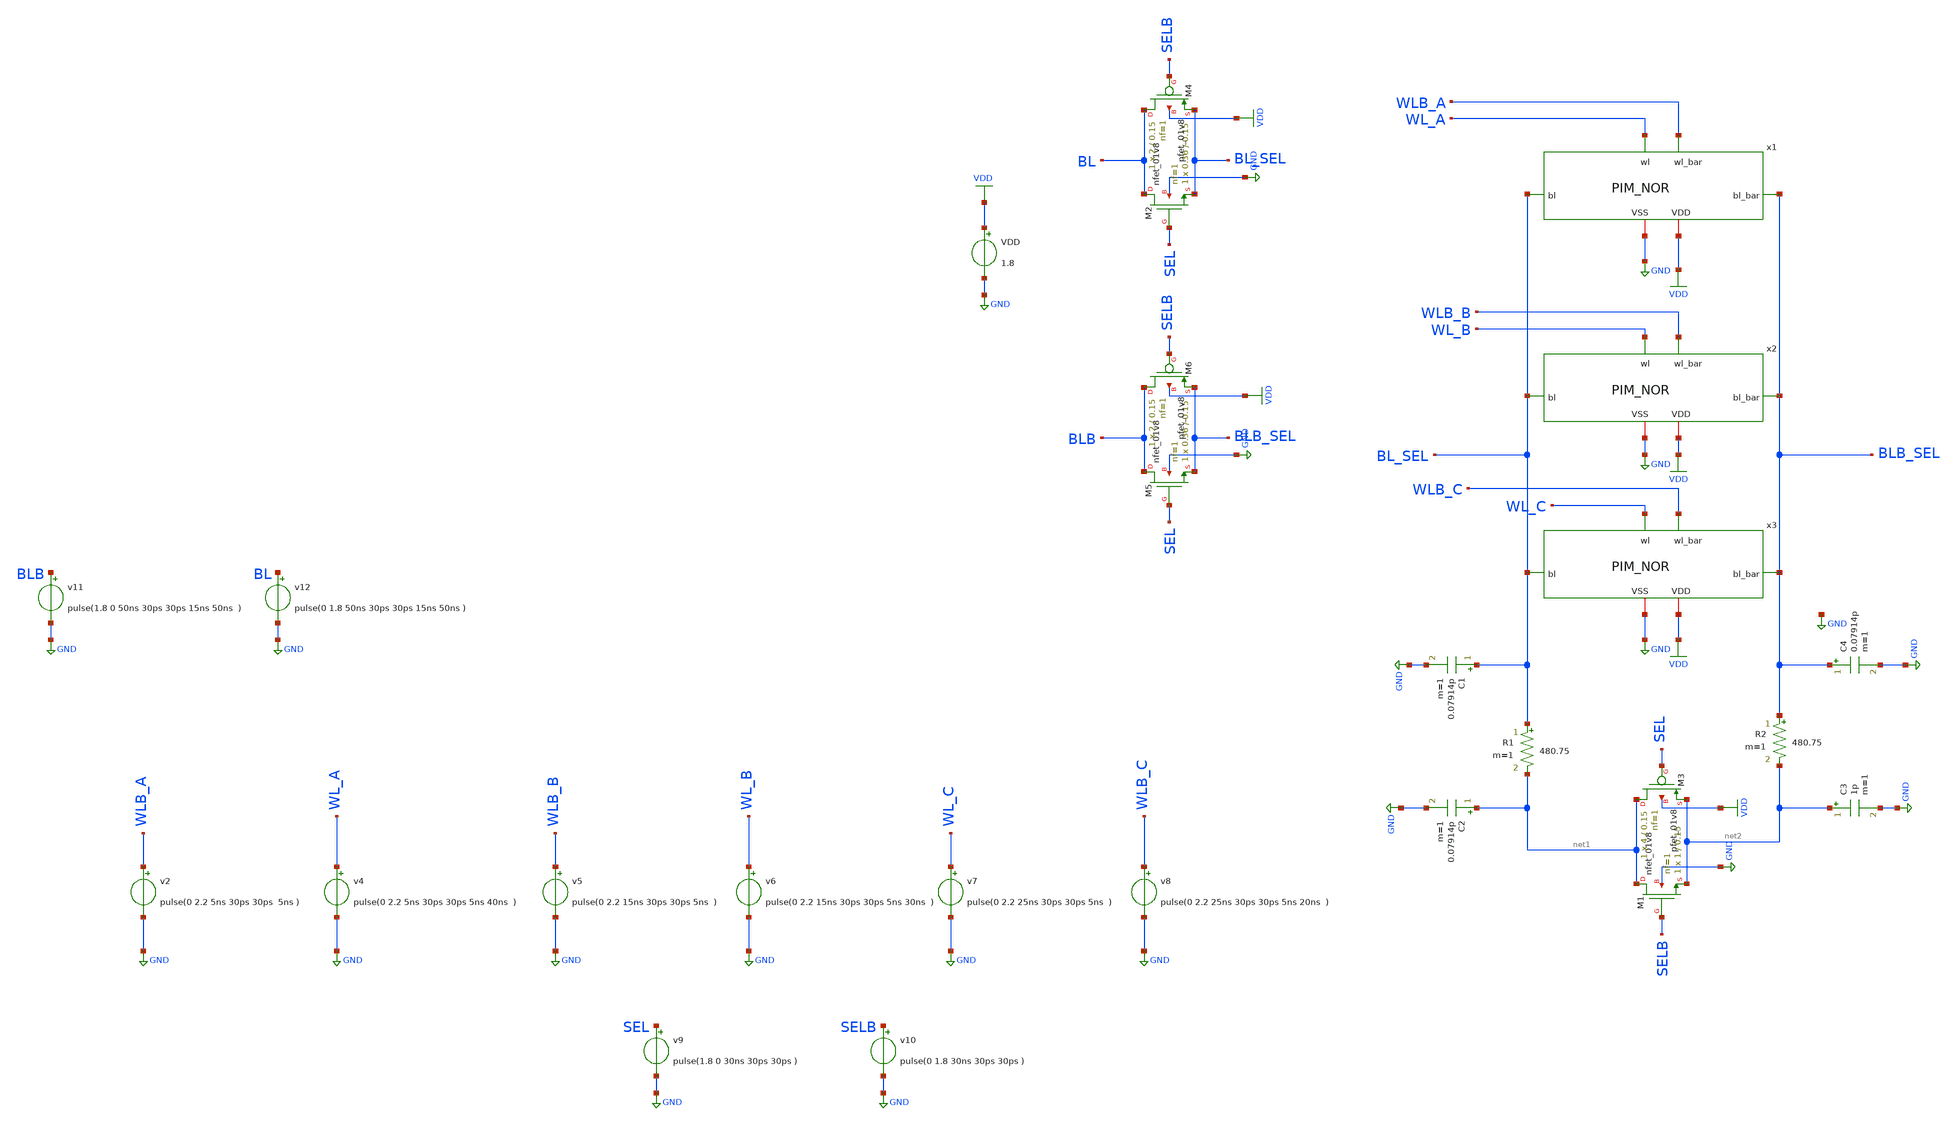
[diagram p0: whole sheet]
** sch_path: nikhil/SRAM/NAND_DEMO_3_res_test_00.sch
**.subckt NAND_DEMO_3_res_test_00
x1 WL_A WLB_A VDD BL_SEL BLB_SEL GND PIM_NOR
x2 WL_B WLB_B VDD BL_SEL BLB_SEL GND PIM_NOR
x3 WL_C WLB_C VDD BL_SEL BLB_SEL GND PIM_NOR
VDD VDD GND 1.8
XM2 BL SEL BL_SEL GND sky130_fd_pr__nfet_01v8 L=0.15 W=0.36 nf=1 ad='int((nf+1)/2) * W/nf * 0.29' as='int((nf+2)/2) * W/nf * 0.29'
+ pd='2*int((nf+1)/2) * (W/nf + 0.29)' ps='2*int((nf+2)/2) * (W/nf + 0.29)' nrd='0.29 / W' nrs='0.29 / W'
+ sa=0 sb=0 sd=0 mult=1 m=1
XM4 BL SELB BL_SEL VDD sky130_fd_pr__pfet_01v8 L=0.15 W=2 nf=1 ad='int((nf+1)/2) * W/nf * 0.29' as='int((nf+2)/2) * W/nf * 0.29'
+ pd='2*int((nf+1)/2) * (W/nf + 0.29)' ps='2*int((nf+2)/2) * (W/nf + 0.29)' nrd='0.29 / W' nrs='0.29 / W'
+ sa=0 sb=0 sd=0 mult=1 m=1
XM5 BLB SEL BLB_SEL GND sky130_fd_pr__nfet_01v8 L=0.15 W=0.36 nf=1 ad='int((nf+1)/2) * W/nf * 0.29' as='int((nf+2)/2) * W/nf * 0.29'
+ pd='2*int((nf+1)/2) * (W/nf + 0.29)' ps='2*int((nf+2)/2) * (W/nf + 0.29)' nrd='0.29 / W' nrs='0.29 / W'
+ sa=0 sb=0 sd=0 mult=1 m=1
XM6 BLB SELB BLB_SEL VDD sky130_fd_pr__pfet_01v8 L=0.15 W=2 nf=1 ad='int((nf+1)/2) * W/nf * 0.29' as='int((nf+2)/2) * W/nf * 0.29'
+ pd='2*int((nf+1)/2) * (W/nf + 0.29)' ps='2*int((nf+2)/2) * (W/nf + 0.29)' nrd='0.29 / W' nrs='0.29 / W'
+ sa=0 sb=0 sd=0 mult=1 m=1
v2 WLB_A GND pulse(0 2.2 5ns 30ps 30ps 5ns )
v4 WL_A GND pulse(0 2.2 5ns 30ps 30ps 5ns 40ns )
v5 WLB_B GND pulse(0 2.2 15ns 30ps 30ps 5ns )
v6 WL_B GND pulse(0 2.2 15ns 30ps 30ps 5ns 30ns )
v7 WL_C GND pulse(0 2.2 25ns 30ps 30ps 5ns )
v8 WLB_C GND pulse(0 2.2 25ns 30ps 30ps 5ns 20ns )
v9 SEL GND pulse(1.8 0 30ns 30ps 30ps )
v10 SELB GND pulse(0 1.8 30ns 30ps 30ps )
XM1 net1 SELB net2 GND sky130_fd_pr__nfet_01v8 L=0.15 W=1 nf=1 ad='int((nf+1)/2) * W/nf * 0.29' as='int((nf+2)/2) * W/nf * 0.29'
+ pd='2*int((nf+1)/2) * (W/nf + 0.29)' ps='2*int((nf+2)/2) * (W/nf + 0.29)' nrd='0.29 / W' nrs='0.29 / W'
+ sa=0 sb=0 sd=0 mult=1 m=1
XM3 net1 SEL net2 VDD sky130_fd_pr__pfet_01v8 L=0.15 W=4 nf=1 ad='int((nf+1)/2) * W/nf * 0.29' as='int((nf+2)/2) * W/nf * 0.29'
+ pd='2*int((nf+1)/2) * (W/nf + 0.29)' ps='2*int((nf+2)/2) * (W/nf + 0.29)' nrd='0.29 / W' nrs='0.29 / W'
+ sa=0 sb=0 sd=0 mult=1 m=1
C1 BL_SEL GND 0.07914p m=1
R1 BL_SEL net1 480.75 m=1
R2 BLB_SEL net2 480.75 m=1
C2 net1 GND 0.07914p m=1
C3 net2 GND 1p m=1
C4 BLB_SEL GND 0.07914p m=1
v11 BLB GND pulse(1.8 0 50ns 30ps 30ps 15ns 50ns )
v12 BL GND pulse(0 1.8 50ns 30ps 30ps 15ns 50ns )
**** begin user architecture code

.tran


.options wnflag=1
.include /pdk/open_pdks/sources/sky130-pdk/libraries/sky130_fd_pr/latest/cells/nfet_01v8/sky130_fd_pr__nfet_01v8__tt.corner.spice
.include /pdk/open_pdks/sources/sky130-pdk/libraries/sky130_fd_pr/latest/cells/nfet_01v8_lvt/sky130_fd_pr__nfet_01v8_lvt__tt.corner.spice
.include /pdk/open_pdks/sources/sky130-pdk/libraries/sky130_fd_pr/latest/cells/pfet_01v8/sky130_fd_pr__pfet_01v8__tt.corner.spice
.include /pdk/open_pdks/sources/sky130-pdk/libraries/sky130_fd_pr/latest/cells/nfet_03v3_nvt/sky130_fd_pr__nfet_03v3_nvt__tt.corner.spice
.include /pdk/open_pdks/sources/sky130-pdk/libraries/sky130_fd_pr/latest/cells/nfet_05v0_nvt/sky130_fd_pr__nfet_05v0_nvt__tt.corner.spice
.include /pdk/open_pdks/sources/sky130-pdk/libraries/sky130_fd_pr/latest/cells/esd_nfet_01v8/sky130_fd_pr__esd_nfet_01v8__tt.corner.spice
.include /pdk/open_pdks/sources/sky130-pdk/libraries/sky130_fd_pr/latest/cells/pfet_01v8_lvt/sky130_fd_pr__pfet_01v8_lvt__tt.corner.spice
.include /pdk/open_pdks/sources/sky130-pdk/libraries/sky130_fd_pr/latest/cells/pfet_01v8_hvt/sky130_fd_pr__pfet_01v8_hvt__tt.corner.spice
.include /pdk/open_pdks/sources/sky130-pdk/libraries/sky130_fd_pr/latest/cells/esd_pfet_g5v0d10v5/sky130_fd_pr__esd_pfet_g5v0d10v5__tt.corner.spice
.include /pdk/open_pdks/sources/sky130-pdk/libraries/sky130_fd_pr/latest/cells/pfet_g5v0d10v5/sky130_fd_pr__pfet_g5v0d10v5__tt.corner.spice
.include /pdk/open_pdks/sources/sky130-pdk/libraries/sky130_fd_pr/latest/cells/pfet_g5v0d16v0/sky130_fd_pr__pfet_g5v0d16v0__tt.corner.spice
.include /pdk/open_pdks/sources/sky130-pdk/libraries/sky130_fd_pr/latest/cells/nfet_g5v0d10v5/sky130_fd_pr__nfet_g5v0d10v5__tt.corner.spice
.include /pdk/open_pdks/sources/sky130-pdk/libraries/sky130_fd_pr/latest/cells/nfet_g5v0d16v0/sky130_fd_pr__nfet_g5v0d16v0__tt_discrete.corner.spice
.include /pdk/open_pdks/sources/sky130-pdk/libraries/sky130_fd_pr/latest/cells/esd_nfet_g5v0d10v5/sky130_fd_pr__esd_nfet_g5v0d10v5__tt.corner.spice
.include /pdk/open_pdks/sources/sky130-pdk/libraries/sky130_fd_pr/latest/models/corners/tt/nonfet.spice
* Mismatch parameters
.include /pdk/open_pdks/sources/sky130-pdk/libraries/sky130_fd_pr/latest/cells/nfet_01v8/sky130_fd_pr__nfet_01v8__mismatch.corner.spice
.include /pdk/open_pdks/sources/sky130-pdk/libraries/sky130_fd_pr/latest/cells/pfet_01v8/sky130_fd_pr__pfet_01v8__mismatch.corner.spice
.include /pdk/open_pdks/sources/sky130-pdk/libraries/sky130_fd_pr/latest/cells/nfet_01v8_lvt/sky130_fd_pr__nfet_01v8_lvt__mismatch.corner.spice
.include /pdk/open_pdks/sources/sky130-pdk/libraries/sky130_fd_pr/latest/cells/pfet_01v8_lvt/sky130_fd_pr__pfet_01v8_lvt__mismatch.corner.spice
.include /pdk/open_pdks/sources/sky130-pdk/libraries/sky130_fd_pr/latest/cells/pfet_01v8_hvt/sky130_fd_pr__pfet_01v8_hvt__mismatch.corner.spice
.include /pdk/open_pdks/sources/sky130-pdk/libraries/sky130_fd_pr/latest/cells/nfet_g5v0d10v5/sky130_fd_pr__nfet_g5v0d10v5__mismatch.corner.spice
.include /pdk/open_pdks/sources/sky130-pdk/libraries/sky130_fd_pr/latest/cells/pfet_g5v0d10v5/sky130_fd_pr__pfet_g5v0d10v5__mismatch.corner.spice
.include /pdk/open_pdks/sources/sky130-pdk/libraries/sky130_fd_pr/latest/cells/nfet_05v0_nvt/sky130_fd_pr__nfet_05v0_nvt__mismatch.corner.spice
.include /pdk/open_pdks/sources/sky130-pdk/libraries/sky130_fd_pr/latest/cells/nfet_03v3_nvt/sky130_fd_pr__nfet_03v3_nvt__mismatch.corner.spice
* Resistor$::SKYWATER_MODELS/Capacitor
.include /pdk/open_pdks/sources/sky130-pdk/libraries/sky130_fd_pr/latest/models/r+c/res_typical__cap_typical.spice
.include /pdk/open_pdks/sources/sky130-pdk/libraries/sky130_fd_pr/latest/models/r+c/res_typical__cap_typical__lin.spice
* Special cells
.include /pdk/open_pdks/sources/sky130-pdk/libraries/sky130_fd_pr/latest/models/corners/tt/specialized_cells.spice
* All models
.include /pdk/open_pdks/sources/sky130-pdk/libraries/sky130_fd_pr/latest/models/all.spice
* Corner
.include /pdk/open_pdks/sources/sky130-pdk/libraries/sky130_fd_pr/latest/models/corners/tt/rf.spice

**** end user architecture code
**.ends

* expanding   symbol:  SRAM/PIM_NOR.sym # of pins=6
** sym_path: nikhil/SRAM/PIM_NOR.sym
** sch_path: nikhil/SRAM/PIM_NOR.sch
.subckt PIM_NOR wl wl_bar VDD bl bl_bar VSS
*.ipin bl
*.ipin wl
*.iopin VSS
*.iopin VDD
*.ipin wl_bar
*.ipin bl_bar
XM2 Qbar Q VSS VSS sky130_fd_pr__nfet_01v8 L=0.15 W=0.36 nf=1 ad='int((nf+1)/2) * W/nf * 0.29' as='int((nf+2)/2) * W/nf * 0.29'
+ pd='2*int((nf+1)/2) * (W/nf + 0.29)' ps='2*int((nf+2)/2) * (W/nf + 0.29)' nrd='0.29 / W' nrs='0.29 / W'
+ sa=0 sb=0 sd=0 mult=1 m=1
XM3 Q Qbar VDD VDD sky130_fd_pr__pfet_01v8 L=0.15 W=0.42 nf=1 ad='int((nf+1)/2) * W/nf * 0.29' as='int((nf+2)/2) * W/nf * 0.29'
+ pd='2*int((nf+1)/2) * (W/nf + 0.29)' ps='2*int((nf+2)/2) * (W/nf + 0.29)' nrd='0.29 / W' nrs='0.29 / W'
+ sa=0 sb=0 sd=0 mult=1 m=1
XM4 Qbar Q VDD VDD sky130_fd_pr__pfet_01v8 L=0.15 W=0.42 nf=1 ad='int((nf+1)/2) * W/nf * 0.29' as='int((nf+2)/2) * W/nf * 0.29'
+ pd='2*int((nf+1)/2) * (W/nf + 0.29)' ps='2*int((nf+2)/2) * (W/nf + 0.29)' nrd='0.29 / W' nrs='0.29 / W'
+ sa=0 sb=0 sd=0 mult=1 m=1
XM5 bl wl Q GND sky130_fd_pr__nfet_01v8 L=0.15 W=0.36 nf=1 ad='int((nf+1)/2) * W/nf * 0.29' as='int((nf+2)/2) * W/nf * 0.29'
+ pd='2*int((nf+1)/2) * (W/nf + 0.29)' ps='2*int((nf+2)/2) * (W/nf + 0.29)' nrd='0.29 / W' nrs='0.29 / W'
+ sa=0 sb=0 sd=0 mult=1 m=1
XM6 bl_bar wl_bar Qbar GND sky130_fd_pr__nfet_01v8 L=0.15 W=0.36 nf=1 ad='int((nf+1)/2) * W/nf * 0.29'
+ as='int((nf+2)/2) * W/nf * 0.29' pd='2*int((nf+1)/2) * (W/nf + 0.29)' ps='2*int((nf+2)/2) * (W/nf + 0.29)'
+ nrd='0.29 / W' nrs='0.29 / W' sa=0 sb=0 sd=0 mult=1 m=1
XM1 Q Qbar VSS VSS sky130_fd_pr__nfet_01v8 L=0.15 W=0.36 nf=1 ad='int((nf+1)/2) * W/nf * 0.29' as='int((nf+2)/2) * W/nf * 0.29'
+ pd='2*int((nf+1)/2) * (W/nf + 0.29)' ps='2*int((nf+2)/2) * (W/nf + 0.29)' nrd='0.29 / W' nrs='0.29 / W'
+ sa=0 sb=0 sd=0 mult=1 m=1
.ends

.GLOBAL VDD
.GLOBAL GND
.end
